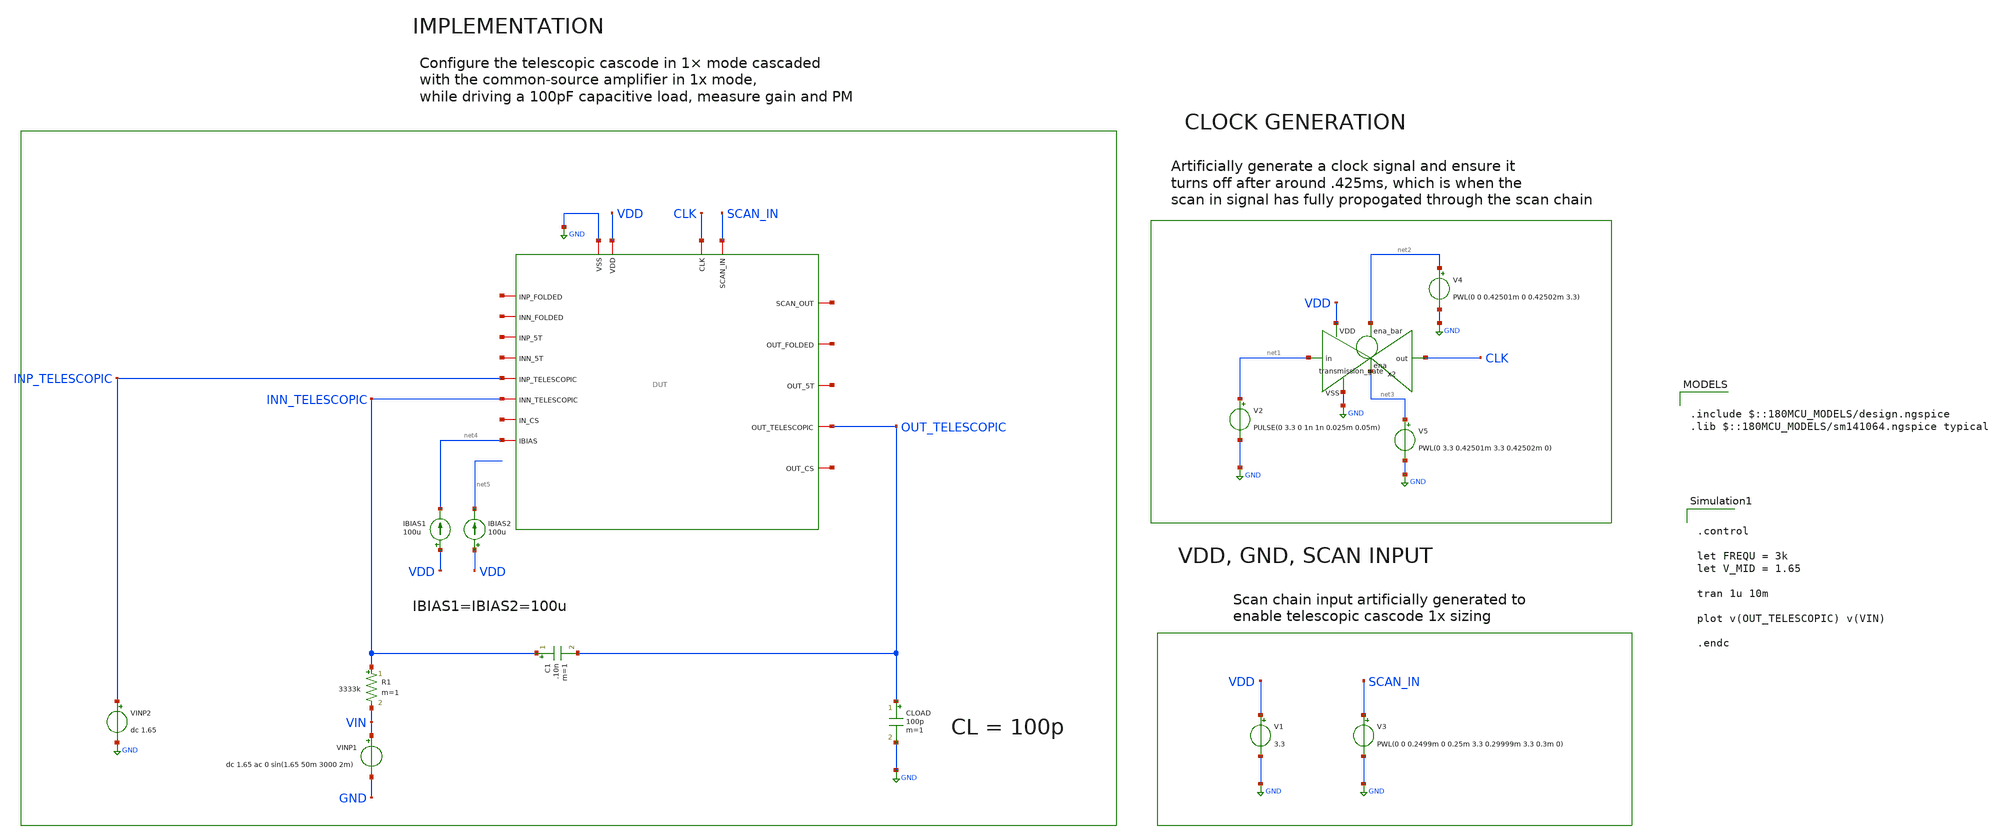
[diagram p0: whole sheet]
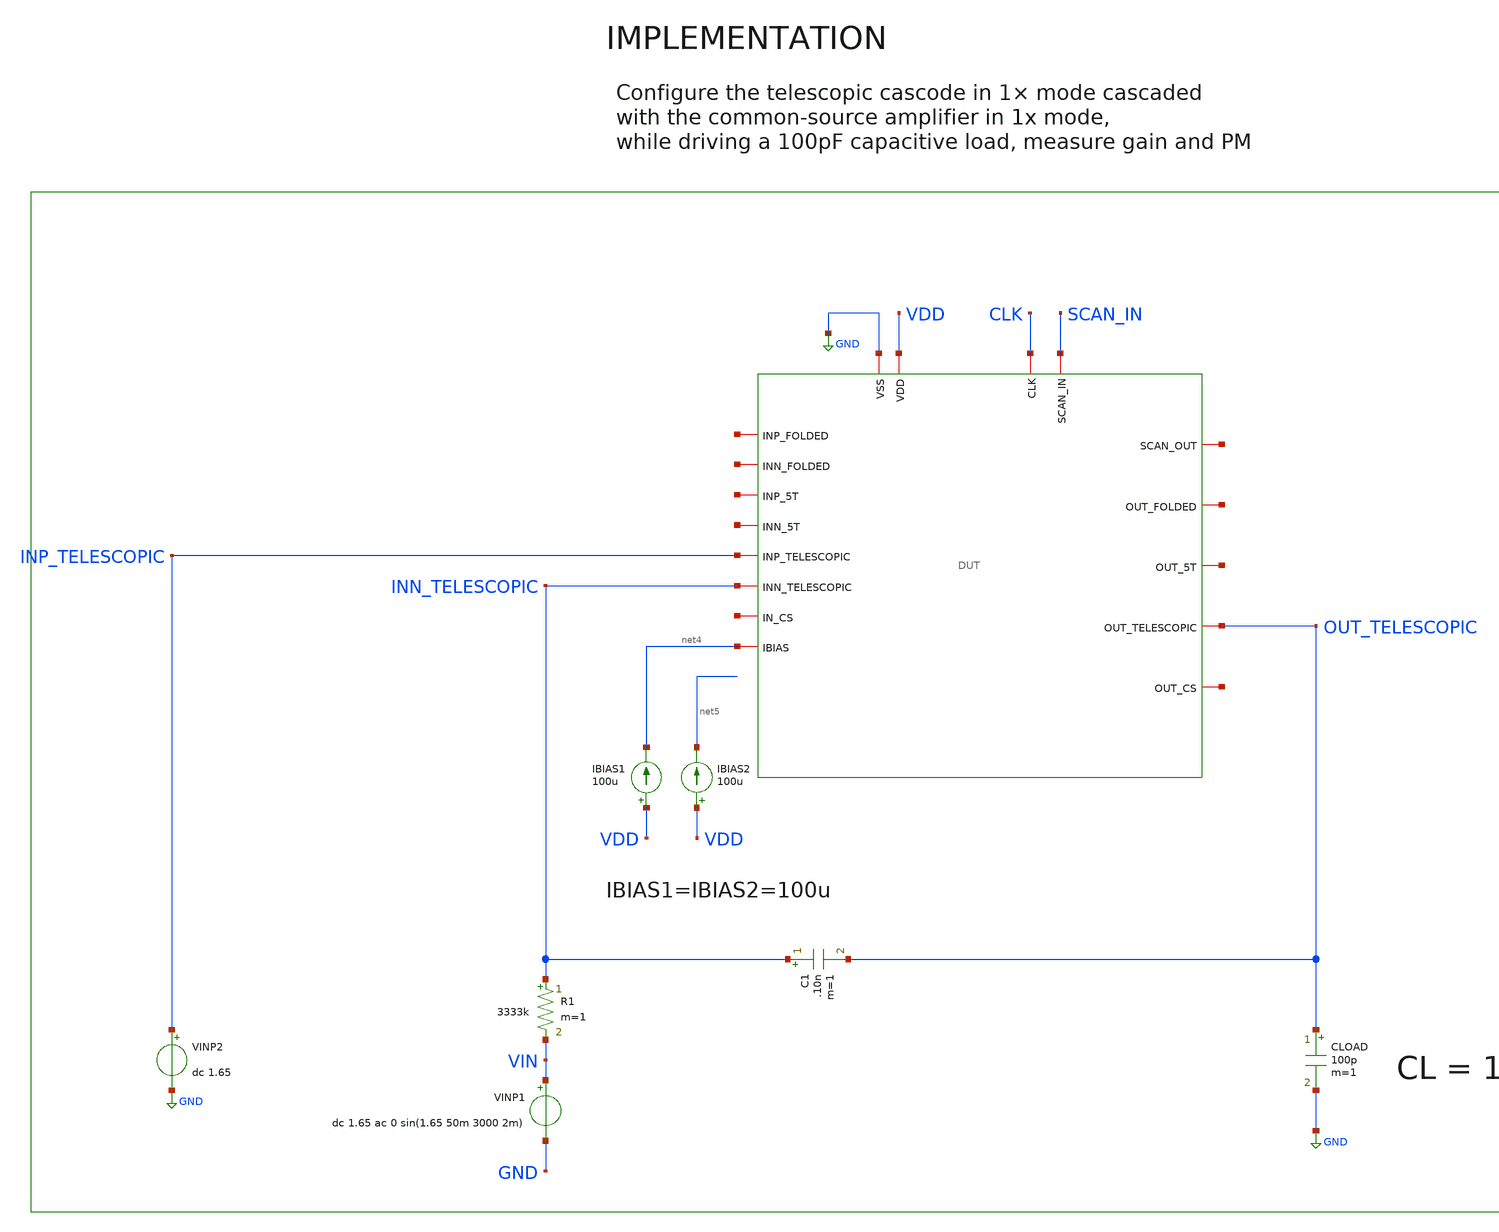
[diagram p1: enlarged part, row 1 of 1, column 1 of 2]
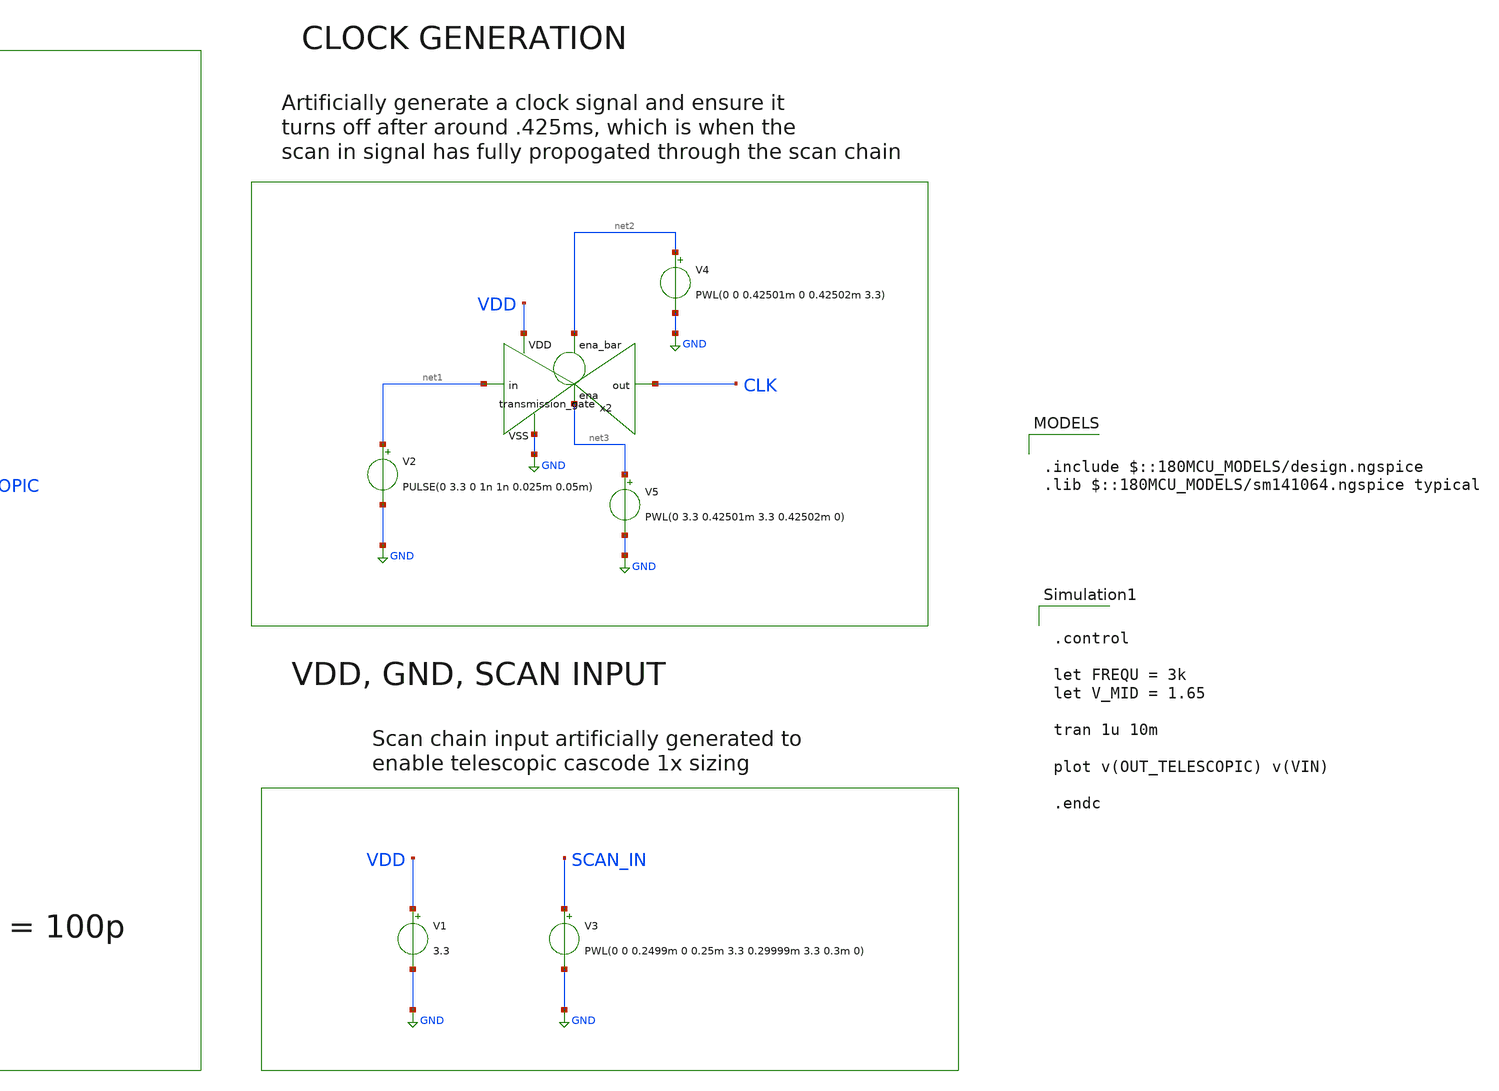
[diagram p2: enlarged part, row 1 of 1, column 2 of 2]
** sch_path: designs/libs/core_tb/mpg/ota_telescopic/integrator.sch
**.subckt integrator
V3 SCAN_IN GND PWL(0 0 0.2499m 0 0.25m 3.3 0.29999m 3.3 0.3m 0)
V1 VDD GND 3.3
V2 net1 GND PULSE(0 3.3 0 1n 1n 0.025m 0.05m)
x2 net2 VDD CLK net1 GND net3 transmission_gate
V4 net2 GND PWL(0 0 0.42501m 0 0.42502m 3.3)
V5 net3 GND PWL(0 3.3 0.42501m 3.3 0.42502m 0)
IBIAS1 VDD net4 100u
IBIAS2 VDD net5 100u
CLOAD OUT_TELESCOPIC GND 100p m=1
x1 CLK net6 SCAN_IN GND VDD net7 net8 net9 net4 net10 net11 net12 INP_TELESCOPIC OUT_TELESCOPIC
+ net13 net14 INN_TELESCOPIC DUT
VINP1 VIN GND dc 1.65 ac 0 sin(1.65 50m 3000 2m)
C1 INN_TELESCOPIC OUT_TELESCOPIC .10n m=1
R1 INN_TELESCOPIC VIN 3333k m=1
VINP2 INP_TELESCOPIC GND dc 1.65
**** begin user architecture code

.include $::180MCU_MODELS/design.ngspice
.lib $::180MCU_MODELS/sm141064.ngspice typical



.control

let FREQU = 3k
let V_MID = 1.65

tran 1u 10m

plot v(OUT_TELESCOPIC) v(VIN)

.endc

**** end user architecture code
**.ends
.GLOBAL GND
.end
